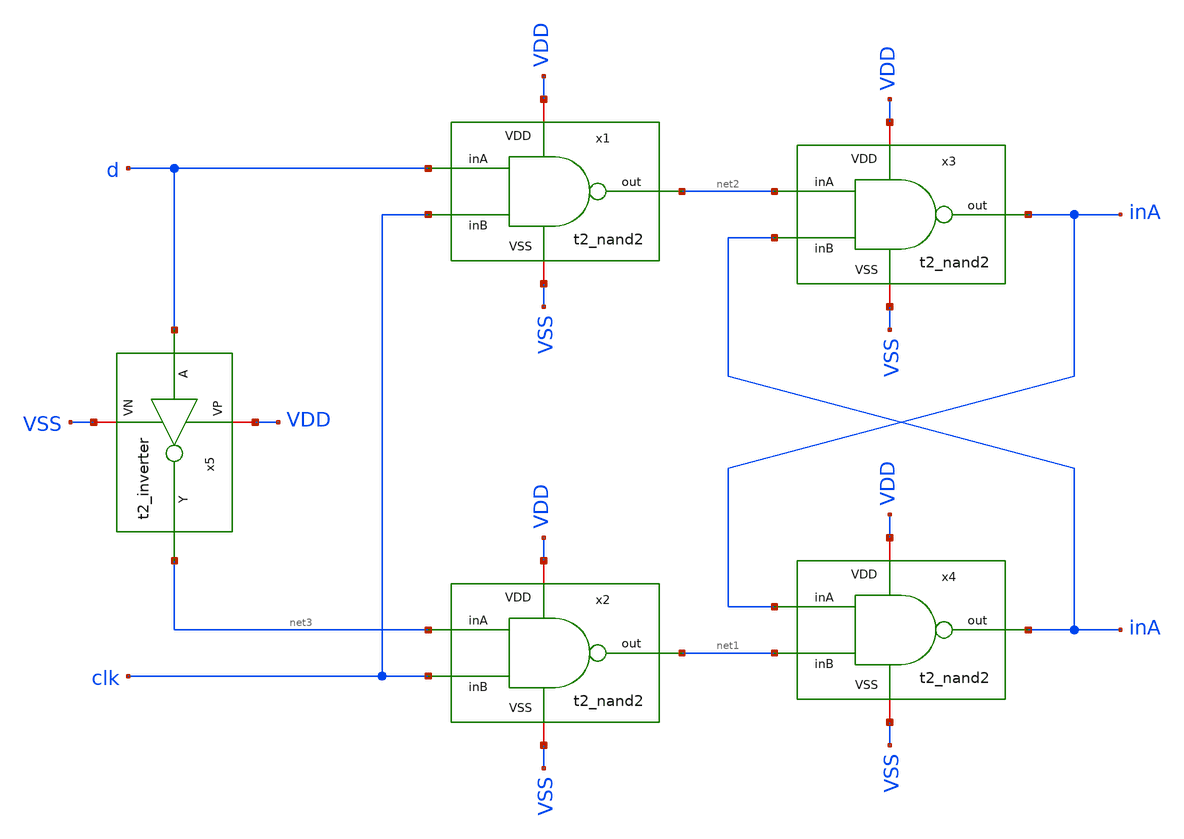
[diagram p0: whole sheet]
** sch_path: Team 2 Design/design_data/xschem/t2_dff.sch
**.subckt t2_dff
x1 VDD d clk net2 VSS t2_nand2
x2 VDD net3 clk net1 VSS t2_nand2
x3 VDD net2 inA inA VSS t2_nand2
x4 VDD inA net1 inA VSS t2_nand2
x5 VDD d net3 VSS t2_inverter
**.ends

* expanding   symbol:  t2_nand2.sym # of pins=5
** sym_path: Team 2 Design/design_data/xschem/t2_nand2.sym
** sch_path: Team 2 Design/design_data/xschem/t2_nand2.sch
.subckt t2_nand2 VDD inA inB out VSS
*.iopin VSS
*.ipin inA
*.ipin inB
*.opin out
*.iopin VDD
XM1 out inA VDD VDD sg13_lv_pmos w=1u l=0.45u ng=1 m=1 mm_ok=1
XM2 out inB VDD VDD sg13_lv_pmos w=1u l=0.45u ng=1 m=1 mm_ok=1
XM3 out inB net1 VSS sg13_lv_nmos w=0.5u l=0.45u ng=1 m=1 mm_ok=1
XM4 net1 inA VSS VSS sg13_lv_nmos w=0.5u l=0.45u ng=1 m=1 mm_ok=1
.ends


* expanding   symbol:  t2_inverter.sym # of pins=4
** sym_path: Team 2 Design/design_data/xschem/t2_inverter.sym
** sch_path: Team 2 Design/design_data/xschem/t2_inverter.sch
.subckt t2_inverter VP A Y VN
*.iopin VP
*.iopin VN
*.ipin A
*.opin Y
XM2 Y A VP VP sg13_lv_pmos w=0.3u l=0.13u ng=1 m=1 mm_ok=1
XM1 Y A VN VN sg13_lv_nmos w=0.15u l=0.13u ng=1 m=1 mm_ok=1
.ends

.end
